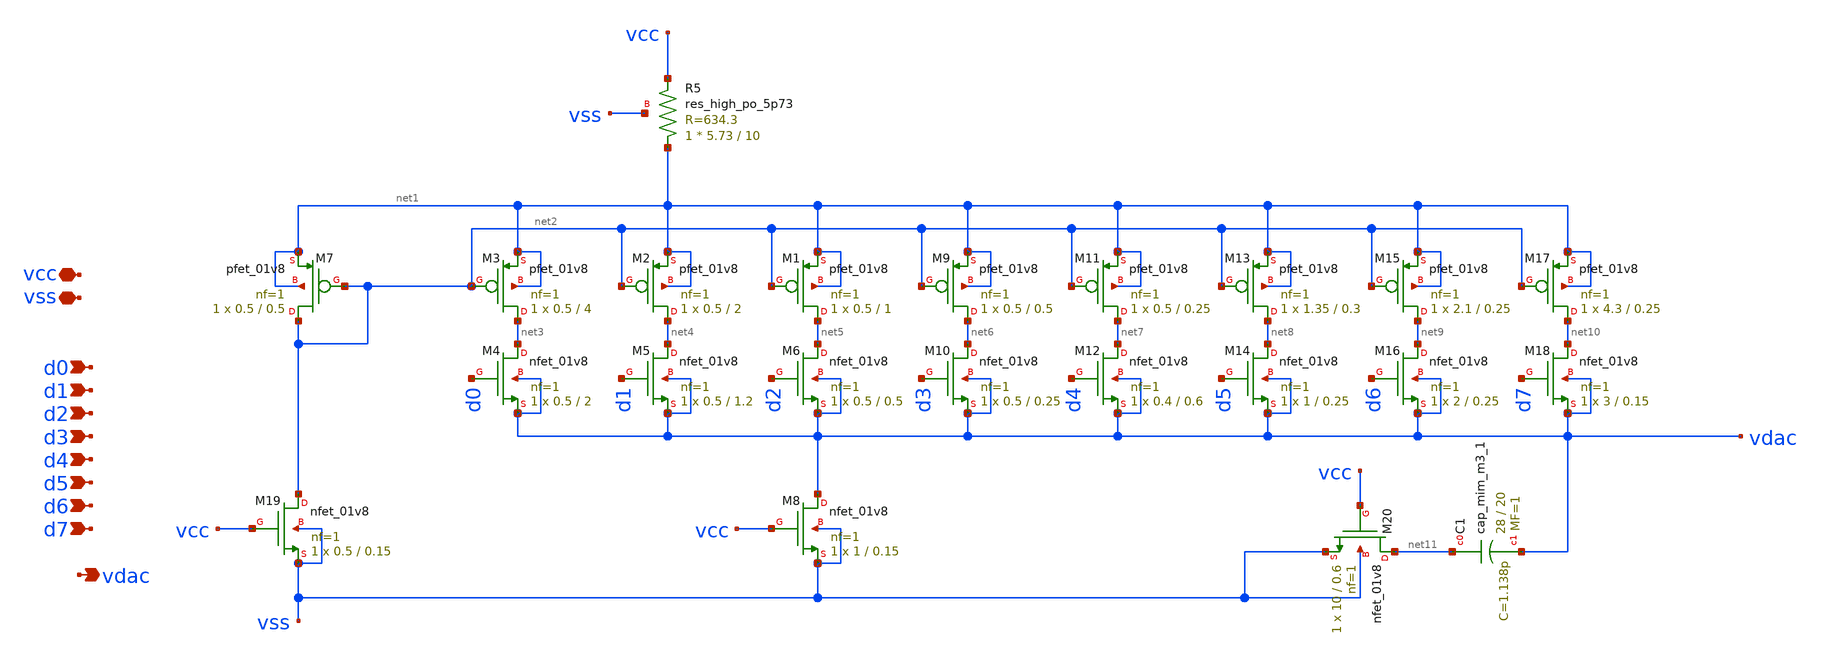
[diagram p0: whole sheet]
** sch_path: xschem/bdac.sch
**.subckt bdac d0 vdac vcc d1 d2 d3 d4 d5 d6 d7 vss
*.ipin d0
*.opin vdac
*.iopin vcc
*.ipin d1
*.ipin d2
*.ipin d3
*.ipin d4
*.ipin d5
*.ipin d6
*.ipin d7
*.iopin vss
XM1 net5 net2 net1 net1 sky130_fd_pr__pfet_01v8 L=1 W=0.5 nf=1 ad='int((nf+1)/2) * W/nf * 0.29' as='int((nf+2)/2) * W/nf * 0.29'
+ pd='2*int((nf+1)/2) * (W/nf + 0.29)' ps='2*int((nf+2)/2) * (W/nf + 0.29)' nrd='0.29 / W' nrs='0.29 / W'
+ sa=0 sb=0 sd=0 mult=1 m=1
XM2 net4 net2 net1 net1 sky130_fd_pr__pfet_01v8 L=2 W=0.5 nf=1 ad='int((nf+1)/2) * W/nf * 0.29' as='int((nf+2)/2) * W/nf * 0.29'
+ pd='2*int((nf+1)/2) * (W/nf + 0.29)' ps='2*int((nf+2)/2) * (W/nf + 0.29)' nrd='0.29 / W' nrs='0.29 / W'
+ sa=0 sb=0 sd=0 mult=1 m=1
XM3 net3 net2 net1 net1 sky130_fd_pr__pfet_01v8 L=4 W=0.5 nf=1 ad='int((nf+1)/2) * W/nf * 0.29' as='int((nf+2)/2) * W/nf * 0.29'
+ pd='2*int((nf+1)/2) * (W/nf + 0.29)' ps='2*int((nf+2)/2) * (W/nf + 0.29)' nrd='0.29 / W' nrs='0.29 / W'
+ sa=0 sb=0 sd=0 mult=1 m=1
XM7 net2 net2 net1 net1 sky130_fd_pr__pfet_01v8 L=0.5 W=0.5 nf=1 ad='int((nf+1)/2) * W/nf * 0.29' as='int((nf+2)/2) * W/nf * 0.29'
+ pd='2*int((nf+1)/2) * (W/nf + 0.29)' ps='2*int((nf+2)/2) * (W/nf + 0.29)' nrd='0.29 / W' nrs='0.29 / W'
+ sa=0 sb=0 sd=0 mult=1 m=1
XM4 net3 d0 vdac vdac sky130_fd_pr__nfet_01v8 L=2 W=0.5 nf=1 ad='int((nf+1)/2) * W/nf * 0.29' as='int((nf+2)/2) * W/nf * 0.29'
+ pd='2*int((nf+1)/2) * (W/nf + 0.29)' ps='2*int((nf+2)/2) * (W/nf + 0.29)' nrd='0.29 / W' nrs='0.29 / W'
+ sa=0 sb=0 sd=0 mult=1 m=1
XM5 net4 d1 vdac vdac sky130_fd_pr__nfet_01v8 L=1.2 W=0.5 nf=1 ad='int((nf+1)/2) * W/nf * 0.29' as='int((nf+2)/2) * W/nf * 0.29'
+ pd='2*int((nf+1)/2) * (W/nf + 0.29)' ps='2*int((nf+2)/2) * (W/nf + 0.29)' nrd='0.29 / W' nrs='0.29 / W'
+ sa=0 sb=0 sd=0 mult=1 m=1
XM6 net5 d2 vdac vdac sky130_fd_pr__nfet_01v8 L=0.5 W=0.5 nf=1 ad='int((nf+1)/2) * W/nf * 0.29' as='int((nf+2)/2) * W/nf * 0.29'
+ pd='2*int((nf+1)/2) * (W/nf + 0.29)' ps='2*int((nf+2)/2) * (W/nf + 0.29)' nrd='0.29 / W' nrs='0.29 / W'
+ sa=0 sb=0 sd=0 mult=1 m=1
XM8 vdac vcc vss vss sky130_fd_pr__nfet_01v8 L=0.15 W=1 nf=1 ad='int((nf+1)/2) * W/nf * 0.29' as='int((nf+2)/2) * W/nf * 0.29'
+ pd='2*int((nf+1)/2) * (W/nf + 0.29)' ps='2*int((nf+2)/2) * (W/nf + 0.29)' nrd='0.29 / W' nrs='0.29 / W'
+ sa=0 sb=0 sd=0 mult=1 m=1
XM9 net6 net2 net1 net1 sky130_fd_pr__pfet_01v8 L=0.5 W=0.5 nf=1 ad='int((nf+1)/2) * W/nf * 0.29' as='int((nf+2)/2) * W/nf * 0.29'
+ pd='2*int((nf+1)/2) * (W/nf + 0.29)' ps='2*int((nf+2)/2) * (W/nf + 0.29)' nrd='0.29 / W' nrs='0.29 / W'
+ sa=0 sb=0 sd=0 mult=1 m=1
XM10 net6 d3 vdac vdac sky130_fd_pr__nfet_01v8 L=0.25 W=0.5 nf=1 ad='int((nf+1)/2) * W/nf * 0.29' as='int((nf+2)/2) * W/nf * 0.29'
+ pd='2*int((nf+1)/2) * (W/nf + 0.29)' ps='2*int((nf+2)/2) * (W/nf + 0.29)' nrd='0.29 / W' nrs='0.29 / W'
+ sa=0 sb=0 sd=0 mult=1 m=1
XM11 net7 net2 net1 net1 sky130_fd_pr__pfet_01v8 L=0.25 W=0.5 nf=1 ad='int((nf+1)/2) * W/nf * 0.29' as='int((nf+2)/2) * W/nf * 0.29'
+ pd='2*int((nf+1)/2) * (W/nf + 0.29)' ps='2*int((nf+2)/2) * (W/nf + 0.29)' nrd='0.29 / W' nrs='0.29 / W'
+ sa=0 sb=0 sd=0 mult=1 m=1
XM12 net7 d4 vdac vdac sky130_fd_pr__nfet_01v8 L=0.6 W=0.4 nf=1 ad='int((nf+1)/2) * W/nf * 0.29' as='int((nf+2)/2) * W/nf * 0.29'
+ pd='2*int((nf+1)/2) * (W/nf + 0.29)' ps='2*int((nf+2)/2) * (W/nf + 0.29)' nrd='0.29 / W' nrs='0.29 / W'
+ sa=0 sb=0 sd=0 mult=1 m=1
XM13 net8 net2 net1 net1 sky130_fd_pr__pfet_01v8 L=0.3 W=1.35 nf=1 ad='int((nf+1)/2) * W/nf * 0.29' as='int((nf+2)/2) * W/nf * 0.29'
+ pd='2*int((nf+1)/2) * (W/nf + 0.29)' ps='2*int((nf+2)/2) * (W/nf + 0.29)' nrd='0.29 / W' nrs='0.29 / W'
+ sa=0 sb=0 sd=0 mult=1 m=1
XM14 net8 d5 vdac vdac sky130_fd_pr__nfet_01v8 L=0.25 W=1 nf=1 ad='int((nf+1)/2) * W/nf * 0.29' as='int((nf+2)/2) * W/nf * 0.29'
+ pd='2*int((nf+1)/2) * (W/nf + 0.29)' ps='2*int((nf+2)/2) * (W/nf + 0.29)' nrd='0.29 / W' nrs='0.29 / W'
+ sa=0 sb=0 sd=0 mult=1 m=1
XM15 net9 net2 net1 net1 sky130_fd_pr__pfet_01v8 L=0.25 W=2.1 nf=1 ad='int((nf+1)/2) * W/nf * 0.29' as='int((nf+2)/2) * W/nf * 0.29'
+ pd='2*int((nf+1)/2) * (W/nf + 0.29)' ps='2*int((nf+2)/2) * (W/nf + 0.29)' nrd='0.29 / W' nrs='0.29 / W'
+ sa=0 sb=0 sd=0 mult=1 m=1
XM16 net9 d6 vdac vdac sky130_fd_pr__nfet_01v8 L=0.25 W=2 nf=1 ad='int((nf+1)/2) * W/nf * 0.29' as='int((nf+2)/2) * W/nf * 0.29'
+ pd='2*int((nf+1)/2) * (W/nf + 0.29)' ps='2*int((nf+2)/2) * (W/nf + 0.29)' nrd='0.29 / W' nrs='0.29 / W'
+ sa=0 sb=0 sd=0 mult=1 m=1
XM17 net10 net2 net1 net1 sky130_fd_pr__pfet_01v8 L=0.25 W=4.3 nf=1 ad='int((nf+1)/2) * W/nf * 0.29'
+ as='int((nf+2)/2) * W/nf * 0.29' pd='2*int((nf+1)/2) * (W/nf + 0.29)' ps='2*int((nf+2)/2) * (W/nf + 0.29)'
+ nrd='0.29 / W' nrs='0.29 / W' sa=0 sb=0 sd=0 mult=1 m=1
XM18 net10 d7 vdac vdac sky130_fd_pr__nfet_01v8 L=0.15 W=3 nf=1 ad='int((nf+1)/2) * W/nf * 0.29' as='int((nf+2)/2) * W/nf * 0.29'
+ pd='2*int((nf+1)/2) * (W/nf + 0.29)' ps='2*int((nf+2)/2) * (W/nf + 0.29)' nrd='0.29 / W' nrs='0.29 / W'
+ sa=0 sb=0 sd=0 mult=1 m=1
XM19 net2 vcc vss vss sky130_fd_pr__nfet_01v8 L=0.15 W=0.5 nf=1 ad='int((nf+1)/2) * W/nf * 0.29' as='int((nf+2)/2) * W/nf * 0.29'
+ pd='2*int((nf+1)/2) * (W/nf + 0.29)' ps='2*int((nf+2)/2) * (W/nf + 0.29)' nrd='0.29 / W' nrs='0.29 / W'
+ sa=0 sb=0 sd=0 mult=1 m=1
XR5 net1 vcc vss sky130_fd_pr__res_high_po_5p73 L=10 mult=1 m=1
XM20 net11 vcc vss vss sky130_fd_pr__nfet_01v8 L=0.6 W=10 nf=1 ad='W * 0.29' as='W * 0.29' pd='2 * (W + 0.29)'
+ ps='2 * (W + 0.29)' nrd='0.29 / W' nrs='0.29 / W' sa=0 sb=0 sd=0 mult=1 m=1
XC1 net11 vdac sky130_fd_pr__cap_mim_m3_1 W=28 L=20 MF=1 m=1
**.ends
.end
